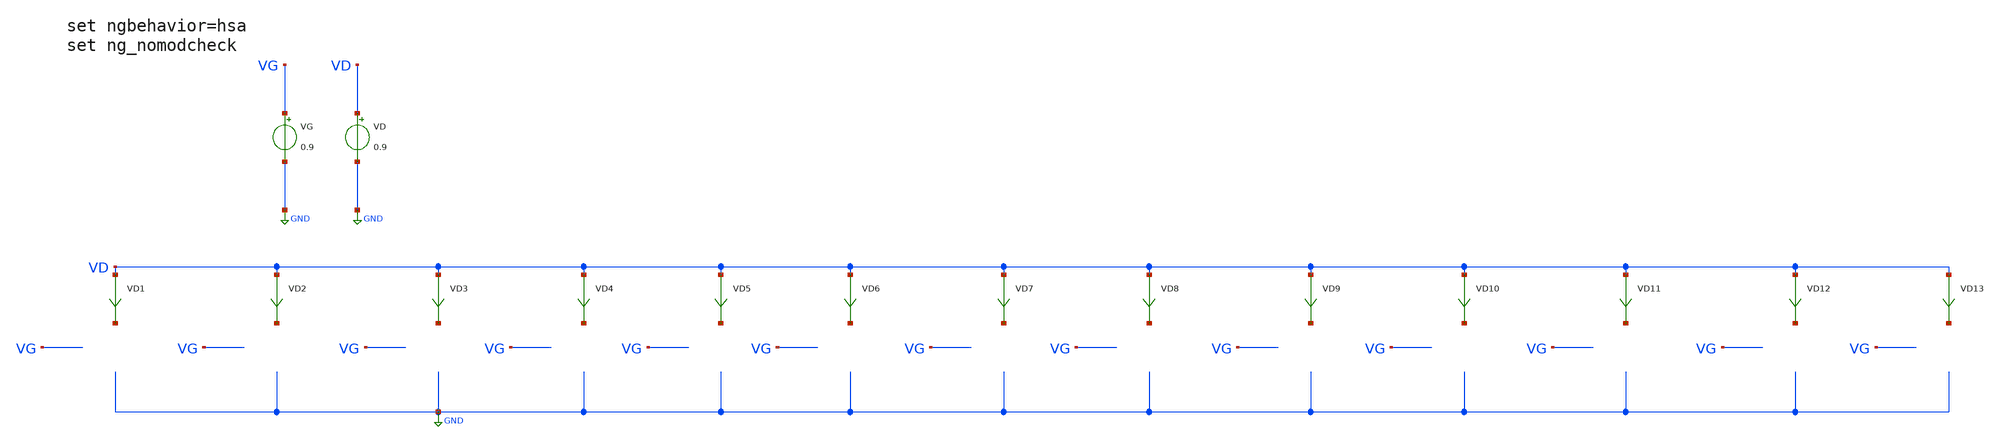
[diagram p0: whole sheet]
** sch_path: Design-Files/gmid_nmos_1v8_hvt_tb.sch
**.subckt gmid_nmos_1v8_hvt_tb
VG VG GND 0.9
VD VD GND 0.9
VD1 VD net1 0
.save i(vd1)
VD2 VD net2 0
.save i(vd2)
VD3 VD net3 0
.save i(vd3)
VD4 VD net4 0
.save i(vd4)
VD5 VD net5 0
.save i(vd5)
VD6 VD net6 0
.save i(vd6)
VD7 VD net7 0
.save i(vd7)
VD8 VD net8 0
.save i(vd8)
VD9 VD net9 0
.save i(vd9)
VD10 VD net10 0
.save i(vd10)
VD11 VD net11 0
.save i(vd11)
VD12 VD net12 0
.save i(vd12)
VD13 VD net13 0
.save i(vd13)
**** begin user architecture code

** opencircuitdesign pdks install
.lib $::SKYWATER_MODELS/sky130.lib.spice ff



* ngspice commands
.option wnflag=1
.option savecurrents
.control
save all
save @m.xm1.msky130_fd_pr__nfet_01v8_hvt[gm]
save @m.xm1.msky130_fd_pr__nfet_01v8_hvt[vth]
save @m.xm1.msky130_fd_pr__nfet_01v8_hvt[gds]
save @m.xm1.msky130_fd_pr__nfet_01v8_hvt[cgg]
save @m.xm1.msky130_fd_pr__nfet_01v8_hvt[cgs]
save @m.xm1.msky130_fd_pr__nfet_01v8_hvt[cgd]
save @m.xm2.msky130_fd_pr__nfet_01v8_hvt[gm]
save @m.xm2.msky130_fd_pr__nfet_01v8_hvt[vth]
save @m.xm2.msky130_fd_pr__nfet_01v8_hvt[gds]
save @m.xm2.msky130_fd_pr__nfet_01v8_hvt[cgg]
save @m.xm2.msky130_fd_pr__nfet_01v8_hvt[cgs]
save @m.xm2.msky130_fd_pr__nfet_01v8_hvt[cgd]
save @m.xm3.msky130_fd_pr__nfet_01v8_hvt[gm]
save @m.xm3.msky130_fd_pr__nfet_01v8_hvt[vth]
save @m.xm3.msky130_fd_pr__nfet_01v8_hvt[gds]
save @m.xm3.msky130_fd_pr__nfet_01v8_hvt[cgg]
save @m.xm3.msky130_fd_pr__nfet_01v8_hvt[cgs]
save @m.xm3.msky130_fd_pr__nfet_01v8_hvt[cgd]
save @m.xm4.msky130_fd_pr__nfet_01v8_hvt[gm]
save @m.xm4.msky130_fd_pr__nfet_01v8_hvt[vth]
save @m.xm4.msky130_fd_pr__nfet_01v8_hvt[gds]
save @m.xm4.msky130_fd_pr__nfet_01v8_hvt[cgg]
save @m.xm4.msky130_fd_pr__nfet_01v8_hvt[cgs]
save @m.xm4.msky130_fd_pr__nfet_01v8_hvt[cgd]
save @m.xm5.msky130_fd_pr__nfet_01v8_hvt[gm]
save @m.xm5.msky130_fd_pr__nfet_01v8_hvt[vth]
save @m.xm5.msky130_fd_pr__nfet_01v8_hvt[gds]
save @m.xm5.msky130_fd_pr__nfet_01v8_hvt[cgg]
save @m.xm5.msky130_fd_pr__nfet_01v8_hvt[cgs]
save @m.xm5.msky130_fd_pr__nfet_01v8_hvt[cgd]
save @m.xm6.msky130_fd_pr__nfet_01v8_hvt[gm]
save @m.xm6.msky130_fd_pr__nfet_01v8_hvt[vth]
save @m.xm6.msky130_fd_pr__nfet_01v8_hvt[gds]
save @m.xm6.msky130_fd_pr__nfet_01v8_hvt[cgg]
save @m.xm6.msky130_fd_pr__nfet_01v8_hvt[cgs]
save @m.xm6.msky130_fd_pr__nfet_01v8_hvt[cgd]
save @m.xm7.msky130_fd_pr__nfet_01v8_hvt[gm]
save @m.xm7.msky130_fd_pr__nfet_01v8_hvt[vth]
save @m.xm7.msky130_fd_pr__nfet_01v8_hvt[gds]
save @m.xm7.msky130_fd_pr__nfet_01v8_hvt[cgg]
save @m.xm7.msky130_fd_pr__nfet_01v8_hvt[cgs]
save @m.xm7.msky130_fd_pr__nfet_01v8_hvt[cgd]
save @m.xm8.msky130_fd_pr__nfet_01v8_hvt[gm]
save @m.xm8.msky130_fd_pr__nfet_01v8_hvt[vth]
save @m.xm8.msky130_fd_pr__nfet_01v8_hvt[gds]
save @m.xm8.msky130_fd_pr__nfet_01v8_hvt[cgg]
save @m.xm8.msky130_fd_pr__nfet_01v8_hvt[cgs]
save @m.xm8.msky130_fd_pr__nfet_01v8_hvt[cgd]
save @m.xm9.msky130_fd_pr__nfet_01v8_hvt[gm]
save @m.xm9.msky130_fd_pr__nfet_01v8_hvt[vth]
save @m.xm9.msky130_fd_pr__nfet_01v8_hvt[gds]
save @m.xm9.msky130_fd_pr__nfet_01v8_hvt[cgg]
save @m.xm9.msky130_fd_pr__nfet_01v8_hvt[cgs]
save @m.xm9.msky130_fd_pr__nfet_01v8_hvt[cgd]
save @m.xm10.msky130_fd_pr__nfet_01v8_hvt[gm]
save @m.xm10.msky130_fd_pr__nfet_01v8_hvt[vth]
save @m.xm10.msky130_fd_pr__nfet_01v8_hvt[gds]
save @m.xm10.msky130_fd_pr__nfet_01v8_hvt[cgg]
save @m.xm10.msky130_fd_pr__nfet_01v8_hvt[cgs]
save @m.xm10.msky130_fd_pr__nfet_01v8_hvt[cgd]
save @m.xm11.msky130_fd_pr__nfet_01v8_hvt[gm]
save @m.xm11.msky130_fd_pr__nfet_01v8_hvt[vth]
save @m.xm11.msky130_fd_pr__nfet_01v8_hvt[gds]
save @m.xm11.msky130_fd_pr__nfet_01v8_hvt[cgg]
save @m.xm11.msky130_fd_pr__nfet_01v8_hvt[cgs]
save @m.xm11.msky130_fd_pr__nfet_01v8_hvt[cgd]
save @m.xm12.msky130_fd_pr__nfet_01v8_hvt[gm]
save @m.xm12.msky130_fd_pr__nfet_01v8_hvt[vth]
save @m.xm12.msky130_fd_pr__nfet_01v8_hvt[gds]
save @m.xm12.msky130_fd_pr__nfet_01v8_hvt[cgg]
save @m.xm12.msky130_fd_pr__nfet_01v8_hvt[cgs]
save @m.xm12.msky130_fd_pr__nfet_01v8_hvt[cgd]
save @m.xm13.msky130_fd_pr__nfet_01v8_hvt[gm]
save @m.xm13.msky130_fd_pr__nfet_01v8_hvt[vth]
save @m.xm13.msky130_fd_pr__nfet_01v8_hvt[gds]
save @m.xm13.msky130_fd_pr__nfet_01v8_hvt[cgg]
save @m.xm13.msky130_fd_pr__nfet_01v8_hvt[cgs]
save @m.xm13.msky130_fd_pr__nfet_01v8_hvt[cgd]
dc VG 0.05 1.8 0.1m
** remove zero length vectors to prevent write errors
remzerovec
write /foss/designs/PDKCHAR/gmid_nmos_svt_tb.raw

plot @m.xm1.msky130_fd_pr__nfet_01v8_hvt[gm]
plot @m.xm2.msky130_fd_pr__nfet_01v8_hvt[gm]
plot @m.xm3.msky130_fd_pr__nfet_01v8_hvt[gm]
plot @m.xm4.msky130_fd_pr__nfet_01v8_hvt[gm]
plot @m.xm5.msky130_fd_pr__nfet_01v8_hvt[gm]
plot @m.xm6.msky130_fd_pr__nfet_01v8_hvt[gm]
plot @m.xm7.msky130_fd_pr__nfet_01v8_hvt[gm]
plot @m.xm8.msky130_fd_pr__nfet_01v8_hvt[gm]
plot @m.xm9.msky130_fd_pr__nfet_01v8_hvt[gm]
plot @m.xm10.msky130_fd_pr__nfet_01v8_hvt[gm]
plot @m.xm11.msky130_fd_pr__nfet_01v8_hvt[gm]
plot @m.xm12.msky130_fd_pr__nfet_01v8_hvt[gm]
plot @m.xm13.msky130_fd_pr__nfet_01v8_hvt[gm]

wrdata /foss/designs/PDKCHAR/gmid_nmos_1_nfet_01v8_hvt_tb.txt
+ @m.xm1.msky130_fd_pr__nfet_01v8_hvt[gm] i(VD1) @m.xm1.msky130_fd_pr__nfet_01v8_hvt[vth] @m.xm1.msky130_fd_pr__nfet_01v8_hvt[gds]
+ @m.xm1.msky130_fd_pr__nfet_01v8_hvt[cgg] @m.xm1.msky130_fd_pr__nfet_01v8_hvt[cgs] @m.xm1.msky130_fd_pr__nfet_01v8_hvt[cgd]
wrdata /foss/designs/PDKCHAR/gmid_nmos_2_nfet_01v8_hvt_tb.txt
+ @m.xm2.msky130_fd_pr__nfet_01v8_hvt[gm] i(VD2) @m.xm2.msky130_fd_pr__nfet_01v8_hvt[vth] @m.xm2.msky130_fd_pr__nfet_01v8_hvt[gds]
+ @m.xm2.msky130_fd_pr__nfet_01v8_hvt[cgg] @m.xm2.msky130_fd_pr__nfet_01v8_hvt[cgs] @m.xm2.msky130_fd_pr__nfet_01v8_hvt[cgd]
wrdata /foss/designs/PDKCHAR/gmid_nmos_3_nfet_01v8_hvt_tb.txt
+ @m.xm3.msky130_fd_pr__nfet_01v8_hvt[gm] i(VD3) @m.xm3.msky130_fd_pr__nfet_01v8_hvt[vth] @m.xm3.msky130_fd_pr__nfet_01v8_hvt[gds]
+ @m.xm3.msky130_fd_pr__nfet_01v8_hvt[cgg] @m.xm3.msky130_fd_pr__nfet_01v8_hvt[cgs] @m.xm3.msky130_fd_pr__nfet_01v8_hvt[cgd]
wrdata /foss/designs/PDKCHAR/gmid_nmos_4_nfet_01v8_hvt_tb.txt
+ @m.xm4.msky130_fd_pr__nfet_01v8_hvt[gm] i(VD4) @m.xm4.msky130_fd_pr__nfet_01v8_hvt[vth] @m.xm4.msky130_fd_pr__nfet_01v8_hvt[gds]
+ @m.xm4.msky130_fd_pr__nfet_01v8_hvt[cgg] @m.xm4.msky130_fd_pr__nfet_01v8_hvt[cgs] @m.xm4.msky130_fd_pr__nfet_01v8_hvt[cgd]
wrdata /foss/designs/PDKCHAR/gmid_nmos_5_nfet_01v8_hvt_tb.txt
+ @m.xm5.msky130_fd_pr__nfet_01v8_hvt[gm] i(VD5) @m.xm5.msky130_fd_pr__nfet_01v8_hvt[vth] @m.xm5.msky130_fd_pr__nfet_01v8_hvt[gds]
+ @m.xm5.msky130_fd_pr__nfet_01v8_hvt[cgg] @m.xm5.msky130_fd_pr__nfet_01v8_hvt[cgs] @m.xm5.msky130_fd_pr__nfet_01v8_hvt[cgd]
wrdata /foss/designs/PDKCHAR/gmid_nmos_6_nfet_01v8_hvt_tb.txt
+ @m.xm6.msky130_fd_pr__nfet_01v8_hvt[gm] i(VD6) @m.xm6.msky130_fd_pr__nfet_01v8_hvt[vth] @m.xm6.msky130_fd_pr__nfet_01v8_hvt[gds]
+ @m.xm6.msky130_fd_pr__nfet_01v8_hvt[cgg] @m.xm6.msky130_fd_pr__nfet_01v8_hvt[cgs] @m.xm6.msky130_fd_pr__nfet_01v8_hvt[cgd]
wrdata /foss/designs/PDKCHAR/gmid_nmos_7_nfet_01v8_hvt_tb.txt
+ @m.xm7.msky130_fd_pr__nfet_01v8_hvt[gm] i(VD7) @m.xm7.msky130_fd_pr__nfet_01v8_hvt[vth] @m.xm7.msky130_fd_pr__nfet_01v8_hvt[gds]
+ @m.xm7.msky130_fd_pr__nfet_01v8_hvt[cgg] @m.xm7.msky130_fd_pr__nfet_01v8_hvt[cgs] @m.xm7.msky130_fd_pr__nfet_01v8_hvt[cgd]
wrdata /foss/designs/PDKCHAR/gmid_nmos_8_nfet_01v8_hvt_tb.txt
+ @m.xm8.msky130_fd_pr__nfet_01v8_hvt[gm] i(VD8) @m.xm8.msky130_fd_pr__nfet_01v8_hvt[vth] @m.xm8.msky130_fd_pr__nfet_01v8_hvt[gds]
+ @m.xm8.msky130_fd_pr__nfet_01v8_hvt[cgg] @m.xm8.msky130_fd_pr__nfet_01v8_hvt[cgs] @m.xm8.msky130_fd_pr__nfet_01v8_hvt[cgd]
wrdata /foss/designs/PDKCHAR/gmid_nmos_9_nfet_01v8_hvt_tb.txt
+ @m.xm9.msky130_fd_pr__nfet_01v8_hvt[gm] i(VD9) @m.xm9.msky130_fd_pr__nfet_01v8_hvt[vth] @m.xm9.msky130_fd_pr__nfet_01v8_hvt[gds]
+ @m.xm9.msky130_fd_pr__nfet_01v8_hvt[cgg] @m.xm9.msky130_fd_pr__nfet_01v8_hvt[cgs] @m.xm9.msky130_fd_pr__nfet_01v8_hvt[cgd]
wrdata /foss/designs/PDKCHAR/gmid_nmos_10_nfet_01v8_hvt_tb.txt
+ @m.xm10.msky130_fd_pr__nfet_01v8_hvt[gm] i(VD10) @m.xm10.msky130_fd_pr__nfet_01v8_hvt[vth] @m.xm10.msky130_fd_pr__nfet_01v8_hvt[gds]
+ @m.xm10.msky130_fd_pr__nfet_01v8_hvt[cgg] @m.xm10.msky130_fd_pr__nfet_01v8_hvt[cgs] @m.xm10.msky130_fd_pr__nfet_01v8_hvt[cgd]
wrdata /foss/designs/PDKCHAR/gmid_nmos_11_nfet_01v8_hvt_tb.txt
+ @m.xm11.msky130_fd_pr__nfet_01v8_hvt[gm] i(VD11) @m.xm11.msky130_fd_pr__nfet_01v8_hvt[vth] @m.xm11.msky130_fd_pr__nfet_01v8_hvt[gds]
+ @m.xm11.msky130_fd_pr__nfet_01v8_hvt[cgg] @m.xm11.msky130_fd_pr__nfet_01v8_hvt[cgs] @m.xm11.msky130_fd_pr__nfet_01v8_hvt[cgd]
wrdata /foss/designs/PDKCHAR/gmid_nmos_12_nfet_01v8_hvt_tb.txt
+ @m.xm12.msky130_fd_pr__nfet_01v8_hvt[gm] i(VD12) @m.xm12.msky130_fd_pr__nfet_01v8_hvt[vth] @m.xm12.msky130_fd_pr__nfet_01v8_hvt[gds]
+ @m.xm12.msky130_fd_pr__nfet_01v8_hvt[cgg] @m.xm12.msky130_fd_pr__nfet_01v8_hvt[cgs] @m.xm12.msky130_fd_pr__nfet_01v8_hvt[cgd]
wrdata /foss/designs/PDKCHAR/gmid_nmos_13_nfet_01v8_hvt_tb.txt
+ @m.xm13.msky130_fd_pr__nfet_01v8_hvt[gm] i(VD13) @m.xm13.msky130_fd_pr__nfet_01v8_hvt[vth] @m.xm13.msky130_fd_pr__nfet_01v8_hvt[gds]
+ @m.xm13.msky130_fd_pr__nfet_01v8_hvt[cgg] @m.xm13.msky130_fd_pr__nfet_01v8_hvt[cgs] @m.xm13.msky130_fd_pr__nfet_01v8_hvt[cgd]
set appendwrite
op
remzerovec
write /foss/designs/PDKCHAR/gmid_nmos_svt_tb.raw
**quit 0
.endc


**** end user architecture code
**.ends
.GLOBAL GND
.end
